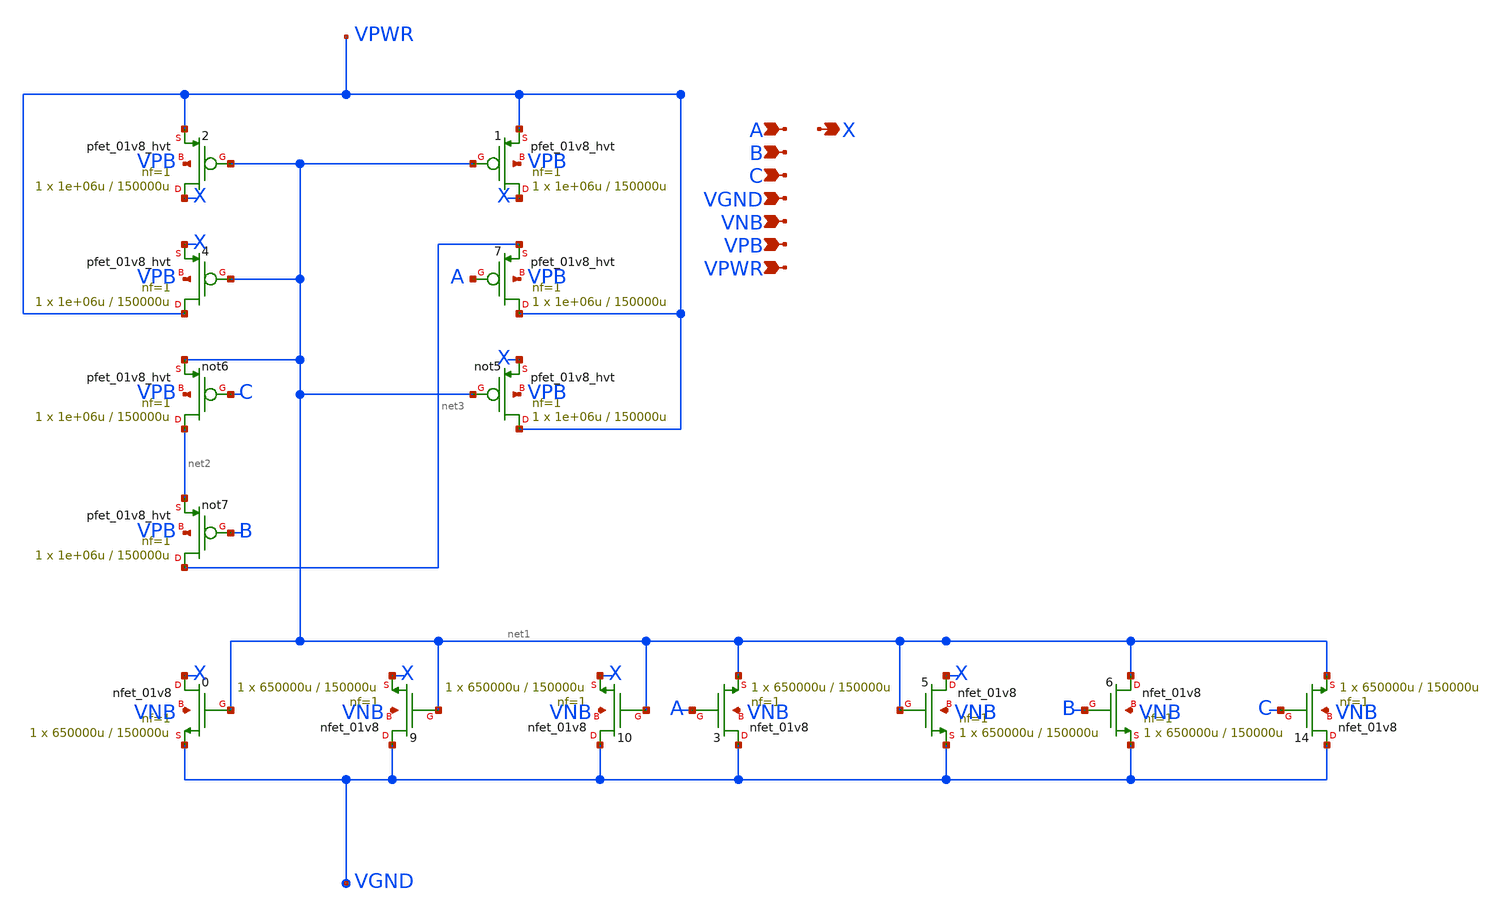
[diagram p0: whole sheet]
** sch_path: schematics/or3/sky130_fd_sc_hd__or3_4.sch
**.subckt sky130_fd_sc_hd__or3_4 A X B VGND VNB VPB VPWR C
*.ipin A
*.opin X
*.ipin B
*.ipin VGND
*.ipin VNB
*.ipin VPB
*.ipin VPWR
*.ipin C
X1 X net1 VPWR VPB sky130_fd_pr__pfet_01v8_hvt L=150000u W=1e+06u nf=1 ad='int((nf+1)/2) * W/nf * 0.29'
+ as='int((nf+2)/2) * W/nf * 0.29' pd='2*int((nf+1)/2) * (W/nf + 0.29)' ps='2*int((nf+2)/2) * (W/nf + 0.29)'
+ nrd='0.29 / W' nrs='0.29 / W' sa=0 sb=0 sd=0 mult=1 m=1
X2 X net1 VPWR VPB sky130_fd_pr__pfet_01v8_hvt L=150000u W=1e+06u nf=1 ad='int((nf+1)/2) * W/nf * 0.29'
+ as='int((nf+2)/2) * W/nf * 0.29' pd='2*int((nf+1)/2) * (W/nf + 0.29)' ps='2*int((nf+2)/2) * (W/nf + 0.29)'
+ nrd='0.29 / W' nrs='0.29 / W' sa=0 sb=0 sd=0 mult=1 m=1
X7 VPWR A net3 VPB sky130_fd_pr__pfet_01v8_hvt L=150000u W=1e+06u nf=1 ad='int((nf+1)/2) * W/nf * 0.29'
+ as='int((nf+2)/2) * W/nf * 0.29' pd='2*int((nf+1)/2) * (W/nf + 0.29)' ps='2*int((nf+2)/2) * (W/nf + 0.29)'
+ nrd='0.29 / W' nrs='0.29 / W' sa=0 sb=0 sd=0 mult=1 m=1
X4 VPWR net1 X VPB sky130_fd_pr__pfet_01v8_hvt L=150000u W=1e+06u nf=1 ad='int((nf+1)/2) * W/nf * 0.29'
+ as='int((nf+2)/2) * W/nf * 0.29' pd='2*int((nf+1)/2) * (W/nf + 0.29)' ps='2*int((nf+2)/2) * (W/nf + 0.29)'
+ nrd='0.29 / W' nrs='0.29 / W' sa=0 sb=0 sd=0 mult=1 m=1
Xnot5 VPWR net1 X VPB sky130_fd_pr__pfet_01v8_hvt L=150000u W=1e+06u nf=1 ad='int((nf+1)/2) * W/nf * 0.29'
+ as='int((nf+2)/2) * W/nf * 0.29' pd='2*int((nf+1)/2) * (W/nf + 0.29)' ps='2*int((nf+2)/2) * (W/nf + 0.29)'
+ nrd='0.29 / W' nrs='0.29 / W' sa=0 sb=0 sd=0 mult=1 m=1
Xnot6 net2 C net1 VPB sky130_fd_pr__pfet_01v8_hvt L=150000u W=1e+06u nf=1 ad='int((nf+1)/2) * W/nf * 0.29'
+ as='int((nf+2)/2) * W/nf * 0.29' pd='2*int((nf+1)/2) * (W/nf + 0.29)' ps='2*int((nf+2)/2) * (W/nf + 0.29)'
+ nrd='0.29 / W' nrs='0.29 / W' sa=0 sb=0 sd=0 mult=1 m=1
Xnot7 net3 B net2 VPB sky130_fd_pr__pfet_01v8_hvt L=150000u W=1e+06u nf=1 ad='int((nf+1)/2) * W/nf * 0.29'
+ as='int((nf+2)/2) * W/nf * 0.29' pd='2*int((nf+1)/2) * (W/nf + 0.29)' ps='2*int((nf+2)/2) * (W/nf + 0.29)'
+ nrd='0.29 / W' nrs='0.29 / W' sa=0 sb=0 sd=0 mult=1 m=1
X0 X net1 VGND VNB sky130_fd_pr__nfet_01v8 L=150000u W=650000u nf=1 ad='int((1 + 1)/2) * 650000u / 1 * 0.29'
+ as='int((1 + 2)/2) * 650000u / 1 * 0.29' pd='2*int((1 + 1)/2) * (650000u / 1 + 0.29)' ps='2*int((1 + 2)/2) * (650000u / 1 + 0.29)'
+ nrd='0.29 / 650000u ' nrs='0.29 / 650000u ' sa=0 sb=0 sd=0 mult=1 m=1
X9 VGND net1 X VNB sky130_fd_pr__nfet_01v8 L=150000u W=650000u nf=1 ad='int((1 + 1)/2) * 650000u / 1 * 0.29'
+ as='int((1 + 2)/2) * 650000u / 1 * 0.29' pd='2*int((1 + 1)/2) * (650000u / 1 + 0.29)' ps='2*int((1 + 2)/2) * (650000u / 1 + 0.29)'
+ nrd='0.29 / 650000u ' nrs='0.29 / 650000u ' sa=0 sb=0 sd=0 mult=1 m=1
X10 VGND net1 X VNB sky130_fd_pr__nfet_01v8 L=150000u W=650000u nf=1 ad='int((1 + 1)/2) * 650000u / 1 * 0.29'
+ as='int((1 + 2)/2) * 650000u / 1 * 0.29' pd='2*int((1 + 1)/2) * (650000u / 1 + 0.29)' ps='2*int((1 + 2)/2) * (650000u / 1 + 0.29)'
+ nrd='0.29 / 650000u ' nrs='0.29 / 650000u ' sa=0 sb=0 sd=0 mult=1 m=1
X3 VGND A net1 VNB sky130_fd_pr__nfet_01v8 L=150000u W=650000u nf=1 ad='int((1 + 1)/2) * 650000u / 1 * 0.29'
+ as='int((1 + 2)/2) * 650000u / 1 * 0.29' pd='2*int((1 + 1)/2) * (650000u / 1 + 0.29)' ps='2*int((1 + 2)/2) * (650000u / 1 + 0.29)'
+ nrd='0.29 / 650000u ' nrs='0.29 / 650000u ' sa=0 sb=0 sd=0 mult=1 m=1
X5 X net1 VGND VNB sky130_fd_pr__nfet_01v8 L=150000u W=650000u nf=1 ad='int((1 + 1)/2) * 650000u / 1 * 0.29'
+ as='int((1 + 2)/2) * 650000u / 1 * 0.29' pd='2*int((1 + 1)/2) * (650000u / 1 + 0.29)' ps='2*int((1 + 2)/2) * (650000u / 1 + 0.29)'
+ nrd='0.29 / 650000u ' nrs='0.29 / 650000u ' sa=0 sb=0 sd=0 mult=1 m=1
X6 net1 B VGND VNB sky130_fd_pr__nfet_01v8 L=150000u W=650000u nf=1 ad='int((1 + 1)/2) * 650000u / 1 * 0.29'
+ as='int((1 + 2)/2) * 650000u / 1 * 0.29' pd='2*int((1 + 1)/2) * (650000u / 1 + 0.29)' ps='2*int((1 + 2)/2) * (650000u / 1 + 0.29)'
+ nrd='0.29 / 650000u ' nrs='0.29 / 650000u ' sa=0 sb=0 sd=0 mult=1 m=1
X14 VGND C net1 VNB sky130_fd_pr__nfet_01v8 L=150000u W=650000u nf=1 ad='int((1 + 1)/2) * 650000u / 1 * 0.29'
+ as='int((1 + 2)/2) * 650000u / 1 * 0.29' pd='2*int((1 + 1)/2) * (650000u / 1 + 0.29)' ps='2*int((1 + 2)/2) * (650000u / 1 + 0.29)'
+ nrd='0.29 / 650000u ' nrs='0.29 / 650000u ' sa=0 sb=0 sd=0 mult=1 m=1
**.ends
.end
